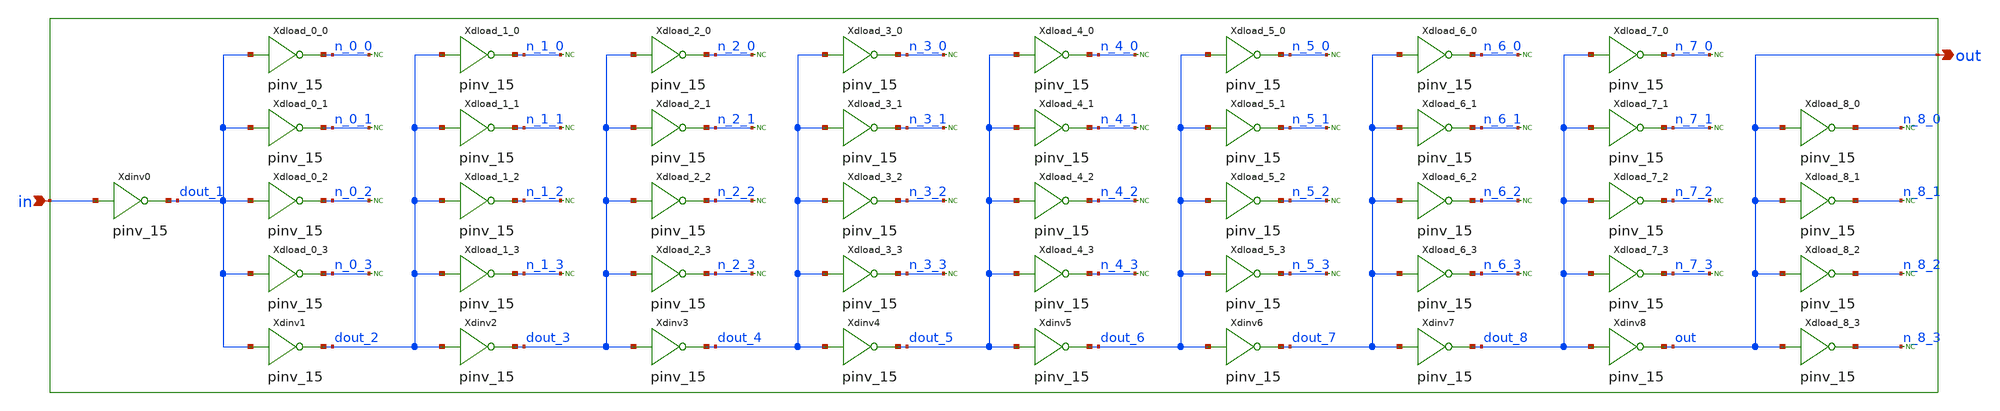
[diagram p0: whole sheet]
** sch_path: sram_2_64_scn4m_lcc/delay_chain.sch
**.subckt delay_chain in out
*.ipin in
*.opin out
Xdinv0 in dout_1 gnd gnd pinv_15
Xdload_0_0 dout_1 n_0_0 gnd gnd pinv_15
Xdload_0_1 dout_1 n_0_1 gnd gnd pinv_15
Xdload_0_2 dout_1 n_0_2 gnd gnd pinv_15
Xdload_0_3 dout_1 n_0_3 gnd gnd pinv_15
Xdinv1 dout_1 dout_2 gnd gnd pinv_15
Xdload_1_0 dout_2 n_1_0 gnd gnd pinv_15
Xdload_1_1 dout_2 n_1_1 gnd gnd pinv_15
Xdload_1_2 dout_2 n_1_2 gnd gnd pinv_15
Xdload_1_3 dout_2 n_1_3 gnd gnd pinv_15
Xdinv2 dout_2 dout_3 gnd gnd pinv_15
Xdload_2_0 dout_3 n_2_0 gnd gnd pinv_15
Xdload_2_1 dout_3 n_2_1 gnd gnd pinv_15
Xdload_2_2 dout_3 n_2_2 gnd gnd pinv_15
Xdload_2_3 dout_3 n_2_3 gnd gnd pinv_15
Xdinv3 dout_3 dout_4 gnd gnd pinv_15
Xdload_3_0 dout_4 n_3_0 gnd gnd pinv_15
Xdload_3_1 dout_4 n_3_1 gnd gnd pinv_15
Xdload_3_2 dout_4 n_3_2 gnd gnd pinv_15
Xdload_3_3 dout_4 n_3_3 gnd gnd pinv_15
Xdinv4 dout_4 dout_5 gnd gnd pinv_15
Xdload_4_0 dout_5 n_4_0 gnd gnd pinv_15
Xdload_4_1 dout_5 n_4_1 gnd gnd pinv_15
Xdload_4_2 dout_5 n_4_2 gnd gnd pinv_15
Xdload_4_3 dout_5 n_4_3 gnd gnd pinv_15
Xdinv5 dout_5 dout_6 gnd gnd pinv_15
Xdload_5_0 dout_6 n_5_0 gnd gnd pinv_15
Xdload_5_1 dout_6 n_5_1 gnd gnd pinv_15
Xdload_5_2 dout_6 n_5_2 gnd gnd pinv_15
Xdload_5_3 dout_6 n_5_3 gnd gnd pinv_15
Xdinv6 dout_6 dout_7 gnd gnd pinv_15
Xdload_6_0 dout_7 n_6_0 gnd gnd pinv_15
Xdload_6_1 dout_7 n_6_1 gnd gnd pinv_15
Xdload_6_2 dout_7 n_6_2 gnd gnd pinv_15
Xdload_6_3 dout_7 n_6_3 gnd gnd pinv_15
Xdinv7 dout_7 dout_8 gnd gnd pinv_15
Xdload_7_0 dout_8 n_7_0 gnd gnd pinv_15
Xdload_7_1 dout_8 n_7_1 gnd gnd pinv_15
Xdload_7_2 dout_8 n_7_2 gnd gnd pinv_15
Xdload_7_3 dout_8 n_7_3 gnd gnd pinv_15
Xdinv8 dout_8 out gnd gnd pinv_15
Xdload_8_0 out n_8_0 gnd gnd pinv_15
Xdload_8_1 out n_8_1 gnd gnd pinv_15
Xdload_8_2 out n_8_2 gnd gnd pinv_15
Xdload_8_3 out n_8_3 gnd gnd pinv_15
* noconn n_0_0
* noconn n_0_1
* noconn n_0_2
* noconn n_0_3
* noconn n_1_0
* noconn n_1_1
* noconn n_1_2
* noconn n_1_3
* noconn n_2_0
* noconn n_2_1
* noconn n_2_2
* noconn n_2_3
* noconn n_3_0
* noconn n_3_1
* noconn n_3_2
* noconn n_3_3
* noconn n_4_0
* noconn n_4_1
* noconn n_4_2
* noconn n_4_3
* noconn n_5_0
* noconn n_5_1
* noconn n_5_2
* noconn n_5_3
* noconn n_6_0
* noconn n_6_1
* noconn n_6_2
* noconn n_6_3
* noconn n_7_0
* noconn n_7_1
* noconn n_7_2
* noconn n_7_3
* noconn n_8_0
* noconn n_8_1
* noconn n_8_2
* noconn n_8_3
**.ends
.end
